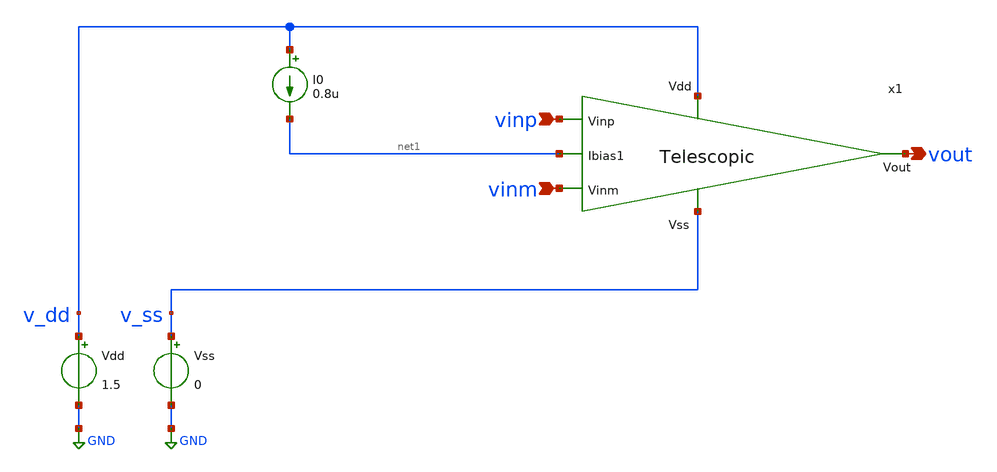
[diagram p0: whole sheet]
** sch_path: design/design_switch_cap/SC_telescop_VCCS.sch
* design/design_switch_cap/Telescopic.sch:
* (c) 2024 Priyanka, @HSB
**.subckt SC_telescop_VCCS vinm vinp vout
*.ipin vinm
*.ipin vinp
*.opin vout
Vss v_ss GND 0
I0 v_dd net1 0.8u
Vdd v_dd GND 1.5
x1 v_dd net1 vout vinm vinp v_ss Telescopic
**.ends

* expanding   symbol:  Telescopic.sym # of pins=6
** sym_path: Telescopic.sym
** sch_path: Telescopic.sch
.subckt Telescopic Vdd Ibias1 Vout Vinm Vinp Vss
*.ipin Vinp
*.opin Vout
*.ipin Vinm
*.ipin Vss
*.ipin Vdd
*.ipin Ibias1
XM19 net1 net7 Vss Vss sg13_lv_nmos w=0.3u l=2u ng=1 m=1 mm_ok=1
XM11 net2 Vinp net1 Vss sg13_lv_nmos w=0.15u l=2u ng=1 m=1 mm_ok=1
XM14 net3 Vinm net1 Vss sg13_lv_nmos w=0.15u l=2u ng=1 m=1 mm_ok=1
XM20 Vout net5 net4 Vdd sg13_lv_pmos w=0.16u l=0.5u ng=1 m=1 mm_ok=1
XM25 net9 net5 net10 Vdd sg13_lv_pmos w=0.16u l=0.5u ng=1 m=1 mm_ok=1
XM1 net5 net7 Vss Vss sg13_lv_nmos w=0.15u l=2u ng=1 m=1 mm_ok=1
XM2 net8 net7 Vss Vss sg13_lv_nmos w=0.15u l=2u ng=1 m=1 mm_ok=1
XM3 Vdd Ibias1 net8 Vss sg13_lv_nmos w=0.15u l=2u ng=1 m=1 mm_ok=1
XM4 Vout Ibias1 net3 Vss sg13_lv_nmos w=0.15u l=2u ng=1 m=1 mm_ok=1
XM5 net9 Ibias1 net2 Vss sg13_lv_nmos w=0.15u l=2u ng=1 m=1 mm_ok=1
XM6 net4 net6 Vdd Vdd sg13_lv_pmos w=0.16u l=0.5u ng=1 m=1 mm_ok=1
XM7 net6 net6 Vdd Vdd sg13_lv_pmos w=0.16u l=0.5u ng=1 m=1 mm_ok=1
XM8 net5 net5 net6 Vdd sg13_lv_pmos w=0.16u l=0.5u ng=1 m=1 mm_ok=1
XM9 net10 net6 Vdd Vdd sg13_lv_pmos w=0.16u l=0.5u ng=1 m=1 mm_ok=1
XM10 net7 net7 Vss Vss sg13_lv_nmos w=0.15u l=2u ng=1 m=1 mm_ok=1
XM12 Ibias1 Ibias1 net7 Vss sg13_lv_nmos w=0.15u l=2u ng=1 m=1 mm_ok=1
.ends

.GLOBAL GND
.end
